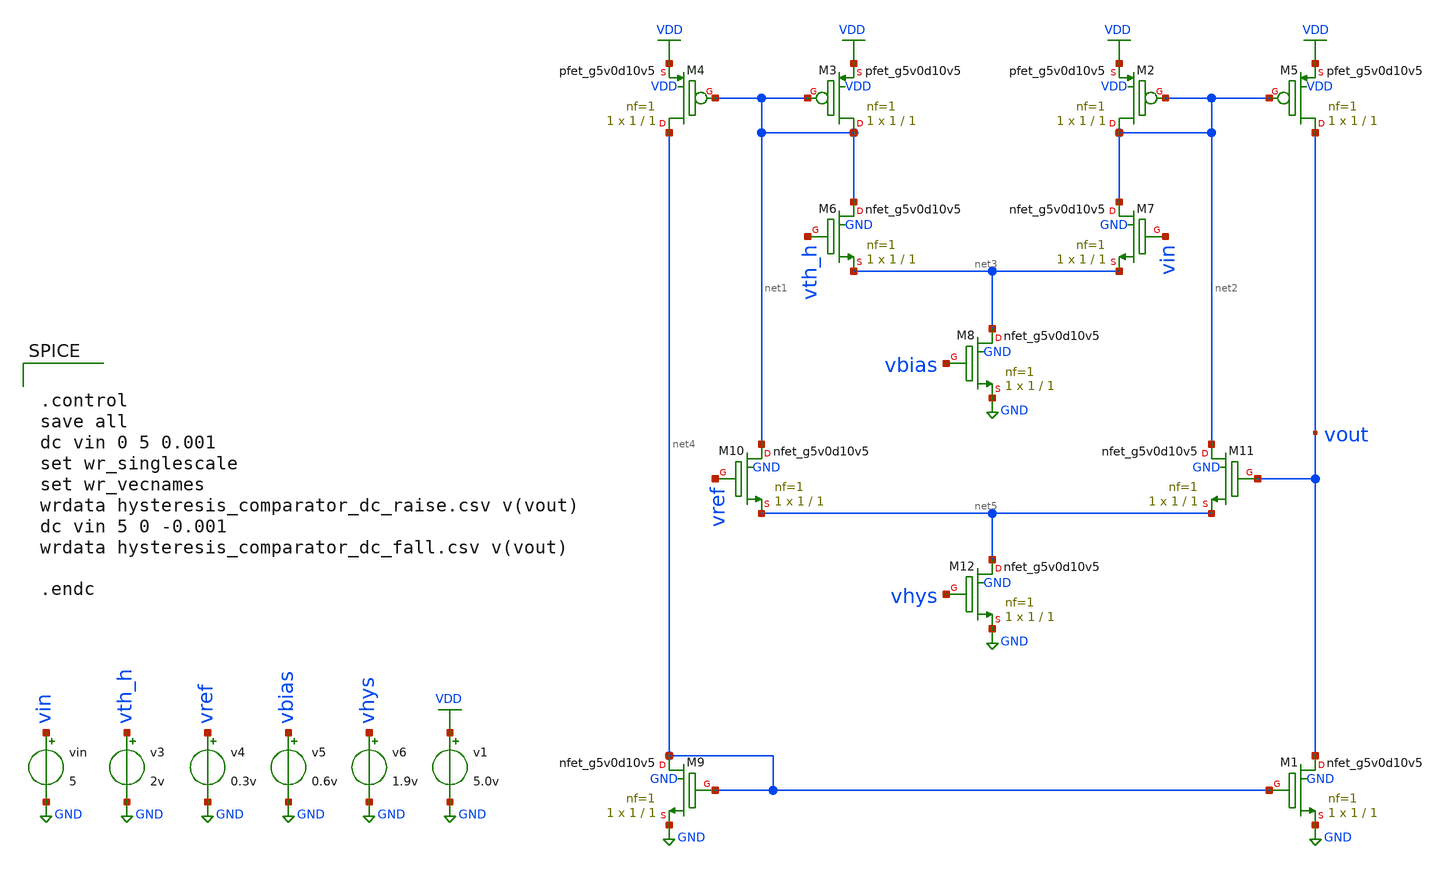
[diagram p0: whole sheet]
** sch_path: schematics/hysteresis_comparator_tb.sch
**.subckt hysteresis_comparator_tb
v1 VDD GND 5.0v
vin vin GND 5
v3 vth_h GND 2v
v4 vref GND 0.3v
v5 vbias GND 0.6v
v6 vhys GND 1.9v
XM3 net1 net1 VDD VDD sky130_fd_pr__pfet_g5v0d10v5 L=1 W=1 nf=1 ad='int((nf+1)/2) * W/nf * 0.29' as='int((nf+2)/2) * W/nf * 0.29'
+ pd='2*int((nf+1)/2) * (W/nf + 0.29)' ps='2*int((nf+2)/2) * (W/nf + 0.29)' nrd='0.29 / W' nrs='0.29 / W'
+ sa=0 sb=0 sd=0 mult=1 m=1
XM1 vout net4 GND GND sky130_fd_pr__nfet_g5v0d10v5 L=1 W=1 nf=1 ad='int((nf+1)/2) * W/nf * 0.29' as='int((nf+2)/2) * W/nf * 0.29'
+ pd='2*int((nf+1)/2) * (W/nf + 0.29)' ps='2*int((nf+2)/2) * (W/nf + 0.29)' nrd='0.29 / W' nrs='0.29 / W'
+ sa=0 sb=0 sd=0 mult=1 m=1
XM2 net2 net2 VDD VDD sky130_fd_pr__pfet_g5v0d10v5 L=1 W=1 nf=1 ad='int((nf+1)/2) * W/nf * 0.29' as='int((nf+2)/2) * W/nf * 0.29'
+ pd='2*int((nf+1)/2) * (W/nf + 0.29)' ps='2*int((nf+2)/2) * (W/nf + 0.29)' nrd='0.29 / W' nrs='0.29 / W'
+ sa=0 sb=0 sd=0 mult=1 m=1
XM4 net4 net1 VDD VDD sky130_fd_pr__pfet_g5v0d10v5 L=1 W=1 nf=1 ad='int((nf+1)/2) * W/nf * 0.29' as='int((nf+2)/2) * W/nf * 0.29'
+ pd='2*int((nf+1)/2) * (W/nf + 0.29)' ps='2*int((nf+2)/2) * (W/nf + 0.29)' nrd='0.29 / W' nrs='0.29 / W'
+ sa=0 sb=0 sd=0 mult=1 m=1
XM5 vout net2 VDD VDD sky130_fd_pr__pfet_g5v0d10v5 L=1 W=1 nf=1 ad='int((nf+1)/2) * W/nf * 0.29' as='int((nf+2)/2) * W/nf * 0.29'
+ pd='2*int((nf+1)/2) * (W/nf + 0.29)' ps='2*int((nf+2)/2) * (W/nf + 0.29)' nrd='0.29 / W' nrs='0.29 / W'
+ sa=0 sb=0 sd=0 mult=1 m=1
XM6 net1 vth_h net3 GND sky130_fd_pr__nfet_g5v0d10v5 L=1 W=1 nf=1 ad='int((nf+1)/2) * W/nf * 0.29' as='int((nf+2)/2) * W/nf * 0.29'
+ pd='2*int((nf+1)/2) * (W/nf + 0.29)' ps='2*int((nf+2)/2) * (W/nf + 0.29)' nrd='0.29 / W' nrs='0.29 / W'
+ sa=0 sb=0 sd=0 mult=1 m=1
XM7 net2 vin net3 GND sky130_fd_pr__nfet_g5v0d10v5 L=1 W=1 nf=1 ad='int((nf+1)/2) * W/nf * 0.29' as='int((nf+2)/2) * W/nf * 0.29'
+ pd='2*int((nf+1)/2) * (W/nf + 0.29)' ps='2*int((nf+2)/2) * (W/nf + 0.29)' nrd='0.29 / W' nrs='0.29 / W'
+ sa=0 sb=0 sd=0 mult=1 m=1
XM8 net3 vbias GND GND sky130_fd_pr__nfet_g5v0d10v5 L=1 W=1 nf=1 ad='int((nf+1)/2) * W/nf * 0.29' as='int((nf+2)/2) * W/nf * 0.29'
+ pd='2*int((nf+1)/2) * (W/nf + 0.29)' ps='2*int((nf+2)/2) * (W/nf + 0.29)' nrd='0.29 / W' nrs='0.29 / W'
+ sa=0 sb=0 sd=0 mult=1 m=1
XM9 net4 net4 GND GND sky130_fd_pr__nfet_g5v0d10v5 L=1 W=1 nf=1 ad='int((nf+1)/2) * W/nf * 0.29' as='int((nf+2)/2) * W/nf * 0.29'
+ pd='2*int((nf+1)/2) * (W/nf + 0.29)' ps='2*int((nf+2)/2) * (W/nf + 0.29)' nrd='0.29 / W' nrs='0.29 / W'
+ sa=0 sb=0 sd=0 mult=1 m=1
XM10 net1 vref net5 GND sky130_fd_pr__nfet_g5v0d10v5 L=1 W=1 nf=1 ad='int((nf+1)/2) * W/nf * 0.29' as='int((nf+2)/2) * W/nf * 0.29'
+ pd='2*int((nf+1)/2) * (W/nf + 0.29)' ps='2*int((nf+2)/2) * (W/nf + 0.29)' nrd='0.29 / W' nrs='0.29 / W'
+ sa=0 sb=0 sd=0 mult=1 m=1
XM11 net2 vout net5 GND sky130_fd_pr__nfet_g5v0d10v5 L=1 W=1 nf=1 ad='int((nf+1)/2) * W/nf * 0.29' as='int((nf+2)/2) * W/nf * 0.29'
+ pd='2*int((nf+1)/2) * (W/nf + 0.29)' ps='2*int((nf+2)/2) * (W/nf + 0.29)' nrd='0.29 / W' nrs='0.29 / W'
+ sa=0 sb=0 sd=0 mult=1 m=1
XM12 net5 vhys GND GND sky130_fd_pr__nfet_g5v0d10v5 L=1 W=1 nf=1 ad='int((nf+1)/2) * W/nf * 0.29' as='int((nf+2)/2) * W/nf * 0.29'
+ pd='2*int((nf+1)/2) * (W/nf + 0.29)' ps='2*int((nf+2)/2) * (W/nf + 0.29)' nrd='0.29 / W' nrs='0.29 / W'
+ sa=0 sb=0 sd=0 mult=1 m=1
**** begin user architecture code


.control
save all
dc vin 0 5 0.001
set wr_singlescale
set wr_vecnames
wrdata hysteresis_comparator_dc_raise.csv v(vout)
dc vin 5 0 -0.001
wrdata hysteresis_comparator_dc_fall.csv v(vout)

.endc


 .lib $::SKYWATER_MODELS/models/sky130.lib.spice tt

.param mc_mm_switch=0
.param mc_pr_switch=1

**** end user architecture code
**.ends
.GLOBAL VDD
.GLOBAL GND
.end
